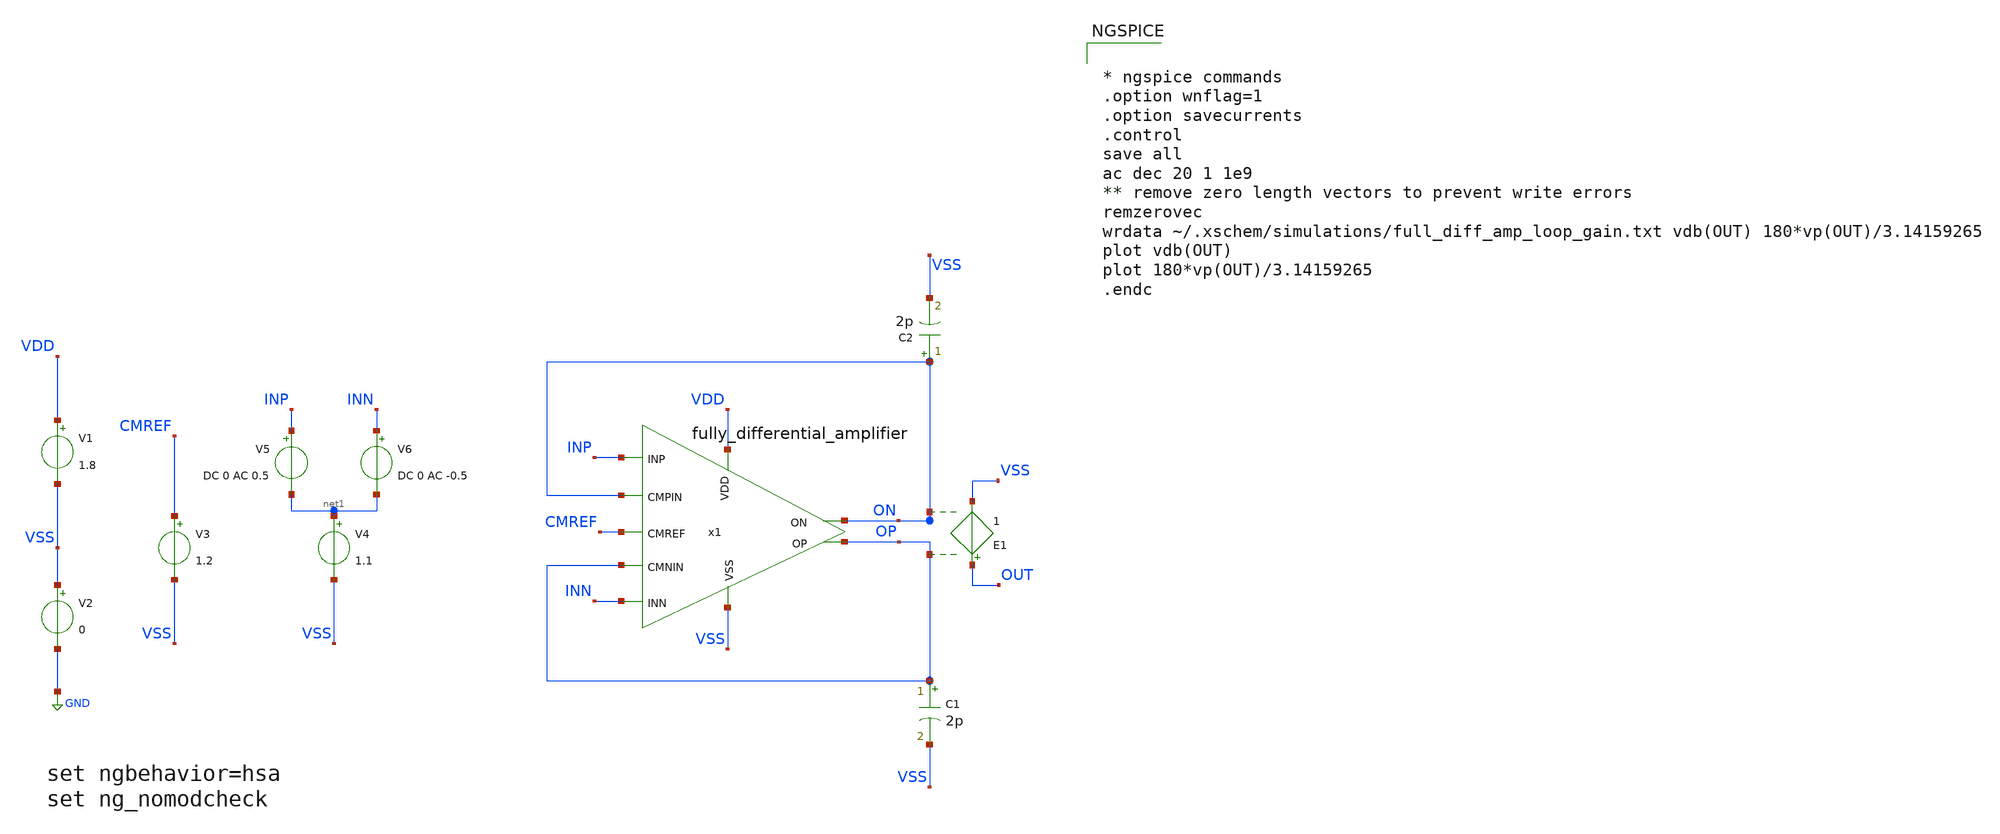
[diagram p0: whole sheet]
** sch_path: testbenches/full_diff_amp_loop_gain.sch
**.subckt full_diff_amp_loop_gain
x1 VDD ON INP OP INN ON OP CMREF VSS fully_differential_amplifier
V1 VDD VSS 1.8
V2 VSS GND 0
V3 CMREF VSS 1.2
V4 net1 VSS 1.1
V5 INP net1 DC 0 AC 0.5
V6 INN net1 DC 0 AC -0.5
E1 OUT VSS OP ON 1
C1 OP VSS 2p m=1
C2 ON VSS 2p m=1
**** begin user architecture code

** opencircuitdesign pdks install
.lib /foss/pdks/sky130A/libs.tech/combined/sky130.corners.lib.spice fslh



* ngspice commands
.option wnflag=1
.option savecurrents
.control
save all
ac dec 20 1 1e9
** remove zero length vectors to prevent write errors
remzerovec
wrdata ~/.xschem/simulations/full_diff_amp_loop_gain.txt vdb(OUT) 180*vp(OUT)/3.14159265
plot vdb(OUT)
plot 180*vp(OUT)/3.14159265
.endc



.control
begin
    let x1 = v(OUT)
    let x = db(x1[0])-3
    let y = db(x1)
    let l = length(y)-1
    let lpv = 0
    let tol = 0
    set units=degrees
    set do_again = 1

    while ($do_again eq 1)
        while (lpv lt l)
            let lpv = lpv+1
            if (abs(y[lpv]-x) lt tol)
                let threedB = mag(frequency[lpv])
                set do_again = 0
            end
        end
        if ($do_again eq 1)
            let tol = tol+0.1
            let lpv = 0
        end
    end
    let tol = 0
    set do_again = 1
    while ($do_again eq 1)
        while (lpv lt l)
            let lpv = lpv+1
            if (abs(y[lpv]) lt tol)
                let UGB = mag(frequency[lpv])
                let PM = 180 + ph(x1[lpv])
                set do_again = 0
            end
        end
        if ($do_again eq 1)
            let tol = tol+0.1
            let lpv = 0
        end
    end

    let DC_Gain = db(x1[0])
    print DC_Gain
    print threedB
    print UGB
    print PM

    label BOTTOM
    unlet x1 x y l lpv threedB UGB DC_Gain PM tol
    unset do_again
end
op
remzerovec
write ~/.xschem/simulations/full_diff_amp_loop_gain.raw
.endc


**** end user architecture code
**.ends

* expanding   symbol:  /foss/designs/sky130_analog_labs/designs/fully_differential_amplifier.sym #
*+ of pins=9
** sym_path: designs/fully_differential_amplifier.sym
** sch_path: designs/fully_differential_amplifier.sch
.subckt fully_differential_amplifier VDD ON INP OP INN CMPIN CMNIN CMREF VSS
*.ipin INP
*.ipin INN
*.ipin VDD
*.ipin VSS
*.opin OP
*.opin ON
*.ipin CMPIN
*.ipin CMNIN
*.ipin CMREF
XM1 net3 PBIAS VDD VDD sky130_fd_pr__pfet_01v8_lvt L=6 W=36 nf=1 ad='int((nf+1)/2) * W/nf * 0.29' as='int((nf+2)/2) * W/nf * 0.29'
+ pd='2*int((nf+1)/2) * (W/nf + 0.29)' ps='2*int((nf+2)/2) * (W/nf + 0.29)' nrd='0.29 / W' nrs='0.29 / W'
+ sa=0 sb=0 sd=0 mult=1 m=1
XM2 net2 PBIAS VDD VDD sky130_fd_pr__pfet_01v8_lvt L=6 W=36 nf=1 ad='int((nf+1)/2) * W/nf * 0.29' as='int((nf+2)/2) * W/nf * 0.29'
+ pd='2*int((nf+1)/2) * (W/nf + 0.29)' ps='2*int((nf+2)/2) * (W/nf + 0.29)' nrd='0.29 / W' nrs='0.29 / W'
+ sa=0 sb=0 sd=0 mult=1 m=1
XQ1 net6 net8 net1 VSS sky130_fd_pr__npn_05v5_w1p00l2p00
XQ2 net5 net8 VSS VSS sky130_fd_pr__npn_05v5_w1p00l2p00
XR1 VSS net1 VSS sky130_fd_pr__res_high_po_1p41 L=260 mult=1 m=1
XM3 PBIAS PCAS net3 VDD sky130_fd_pr__pfet_01v8_lvt L=6 W=36 nf=1 ad='int((nf+1)/2) * W/nf * 0.29' as='int((nf+2)/2) * W/nf * 0.29'
+ pd='2*int((nf+1)/2) * (W/nf + 0.29)' ps='2*int((nf+2)/2) * (W/nf + 0.29)' nrd='0.29 / W' nrs='0.29 / W'
+ sa=0 sb=0 sd=0 mult=4 m=4
XM7 net4 PCAS net2 VDD sky130_fd_pr__pfet_01v8_lvt L=6 W=36 nf=1 ad='int((nf+1)/2) * W/nf * 0.29' as='int((nf+2)/2) * W/nf * 0.29'
+ pd='2*int((nf+1)/2) * (W/nf + 0.29)' ps='2*int((nf+2)/2) * (W/nf + 0.29)' nrd='0.29 / W' nrs='0.29 / W'
+ sa=0 sb=0 sd=0 mult=4 m=4
XR7 PCAS PBIAS VSS sky130_fd_pr__res_high_po_1p41 L=600 mult=1 m=1
XR8 net7 net4 VSS sky130_fd_pr__res_high_po_1p41 L=600 mult=1 m=1
XM16 net7 net8 net5 VSS sky130_fd_pr__nfet_05v0_nvt L=2 W=10 nf=1 ad='int((nf+1)/2) * W/nf * 0.29' as='int((nf+2)/2) * W/nf * 0.29'
+ pd='2*int((nf+1)/2) * (W/nf + 0.29)' ps='2*int((nf+2)/2) * (W/nf + 0.29)' nrd='0.29 / W' nrs='0.29 / W'
+ sa=0 sb=0 sd=0 mult=6 m=6
XM18 PCAS net8 net6 VSS sky130_fd_pr__nfet_05v0_nvt L=2 W=10 nf=1 ad='int((nf+1)/2) * W/nf * 0.29' as='int((nf+2)/2) * W/nf * 0.29'
+ pd='2*int((nf+1)/2) * (W/nf + 0.29)' ps='2*int((nf+2)/2) * (W/nf + 0.29)' nrd='0.29 / W' nrs='0.29 / W'
+ sa=0 sb=0 sd=0 mult=6 m=6
XM19 VDD net7 net8 VSS sky130_fd_pr__nfet_05v0_nvt L=2 W=10 nf=1 ad='int((nf+1)/2) * W/nf * 0.29' as='int((nf+2)/2) * W/nf * 0.29'
+ pd='2*int((nf+1)/2) * (W/nf + 0.29)' ps='2*int((nf+2)/2) * (W/nf + 0.29)' nrd='0.29 / W' nrs='0.29 / W'
+ sa=0 sb=0 sd=0 mult=1 m=1
XM17 net11 PBIAS VDD VDD sky130_fd_pr__pfet_01v8_lvt L=6 W=36 nf=1 ad='int((nf+1)/2) * W/nf * 0.29' as='int((nf+2)/2) * W/nf * 0.29'
+ pd='2*int((nf+1)/2) * (W/nf + 0.29)' ps='2*int((nf+2)/2) * (W/nf + 0.29)' nrd='0.29 / W' nrs='0.29 / W'
+ sa=0 sb=0 sd=0 mult=1 m=1
XM20 net9 net11 PBIAS VDD sky130_fd_pr__pfet_01v8_lvt L=6 W=10 nf=1 ad='int((nf+1)/2) * W/nf * 0.29'
+ as='int((nf+2)/2) * W/nf * 0.29' pd='2*int((nf+1)/2) * (W/nf + 0.29)' ps='2*int((nf+2)/2) * (W/nf + 0.29)'
+ nrd='0.29 / W' nrs='0.29 / W' sa=0 sb=0 sd=0 mult=1 m=1
XM21 VSS net10 net9 VDD sky130_fd_pr__pfet_01v8_lvt L=6 W=10 nf=1 ad='int((nf+1)/2) * W/nf * 0.29' as='int((nf+2)/2) * W/nf * 0.29'
+ pd='2*int((nf+1)/2) * (W/nf + 0.29)' ps='2*int((nf+2)/2) * (W/nf + 0.29)' nrd='0.29 / W' nrs='0.29 / W'
+ sa=0 sb=0 sd=0 mult=1 m=1
XR10 net10 net11 VSS sky130_fd_pr__res_xhigh_po_0p35 L=350 mult=1 m=1
XR11 VSS net10 VSS sky130_fd_pr__res_xhigh_po_0p35 L=350 mult=1 m=1
XM4 net17 PBIAS VDD VDD sky130_fd_pr__pfet_01v8_lvt L=6 W=36 nf=1 ad='int((nf+1)/2) * W/nf * 0.29' as='int((nf+2)/2) * W/nf * 0.29'
+ pd='2*int((nf+1)/2) * (W/nf + 0.29)' ps='2*int((nf+2)/2) * (W/nf + 0.29)' nrd='0.29 / W' nrs='0.29 / W'
+ sa=0 sb=0 sd=0 mult=1 m=1
XM5 NCAS PCAS net17 VDD sky130_fd_pr__pfet_01v8_lvt L=6 W=36 nf=1 ad='int((nf+1)/2) * W/nf * 0.29' as='int((nf+2)/2) * W/nf * 0.29'
+ pd='2*int((nf+1)/2) * (W/nf + 0.29)' ps='2*int((nf+2)/2) * (W/nf + 0.29)' nrd='0.29 / W' nrs='0.29 / W'
+ sa=0 sb=0 sd=0 mult=4 m=4
XR2 NBIAS NCAS VSS sky130_fd_pr__res_high_po_1p41 L=600 mult=1 m=1
XM6 NBIAS NCAS net12 VSS sky130_fd_pr__nfet_01v8 L=6 W=36 nf=1 ad='int((nf+1)/2) * W/nf * 0.29' as='int((nf+2)/2) * W/nf * 0.29'
+ pd='2*int((nf+1)/2) * (W/nf + 0.29)' ps='2*int((nf+2)/2) * (W/nf + 0.29)' nrd='0.29 / W' nrs='0.29 / W'
+ sa=0 sb=0 sd=0 mult=4 m=4
XM8 net12 NBIAS VSS VSS sky130_fd_pr__nfet_01v8 L=6 W=36 nf=1 ad='int((nf+1)/2) * W/nf * 0.29' as='int((nf+2)/2) * W/nf * 0.29'
+ pd='2*int((nf+1)/2) * (W/nf + 0.29)' ps='2*int((nf+2)/2) * (W/nf + 0.29)' nrd='0.29 / W' nrs='0.29 / W'
+ sa=0 sb=0 sd=0 mult=1 m=1
XM9 net18 INN net14 VSS sky130_fd_pr__nfet_01v8 L=1 W=150 nf=1 ad='int((nf+1)/2) * W/nf * 0.29' as='int((nf+2)/2) * W/nf * 0.29'
+ pd='2*int((nf+1)/2) * (W/nf + 0.29)' ps='2*int((nf+2)/2) * (W/nf + 0.29)' nrd='0.29 / W' nrs='0.29 / W'
+ sa=0 sb=0 sd=0 mult=2 m=2
XM10 net19 INP net14 VSS sky130_fd_pr__nfet_01v8 L=1 W=150 nf=1 ad='int((nf+1)/2) * W/nf * 0.29' as='int((nf+2)/2) * W/nf * 0.29'
+ pd='2*int((nf+1)/2) * (W/nf + 0.29)' ps='2*int((nf+2)/2) * (W/nf + 0.29)' nrd='0.29 / W' nrs='0.29 / W'
+ sa=0 sb=0 sd=0 mult=2 m=2
XM11 net14 NCAS net13 VSS sky130_fd_pr__nfet_01v8 L=6 W=36 nf=1 ad='int((nf+1)/2) * W/nf * 0.29' as='int((nf+2)/2) * W/nf * 0.29'
+ pd='2*int((nf+1)/2) * (W/nf + 0.29)' ps='2*int((nf+2)/2) * (W/nf + 0.29)' nrd='0.29 / W' nrs='0.29 / W'
+ sa=0 sb=0 sd=0 mult=84 m=84
XM12 net13 NBIAS VSS VSS sky130_fd_pr__nfet_01v8 L=6 W=36 nf=1 ad='int((nf+1)/2) * W/nf * 0.29' as='int((nf+2)/2) * W/nf * 0.29'
+ pd='2*int((nf+1)/2) * (W/nf + 0.29)' ps='2*int((nf+2)/2) * (W/nf + 0.29)' nrd='0.29 / W' nrs='0.29 / W'
+ sa=0 sb=0 sd=0 mult=21 m=21
XM13 ON NCAS net15 VSS sky130_fd_pr__nfet_01v8 L=6 W=36 nf=1 ad='int((nf+1)/2) * W/nf * 0.29' as='int((nf+2)/2) * W/nf * 0.29'
+ pd='2*int((nf+1)/2) * (W/nf + 0.29)' ps='2*int((nf+2)/2) * (W/nf + 0.29)' nrd='0.29 / W' nrs='0.29 / W'
+ sa=0 sb=0 sd=0 mult=16 m=16
XM14 net15 NBIAS VSS VSS sky130_fd_pr__nfet_01v8 L=6 W=36 nf=1 ad='int((nf+1)/2) * W/nf * 0.29' as='int((nf+2)/2) * W/nf * 0.29'
+ pd='2*int((nf+1)/2) * (W/nf + 0.29)' ps='2*int((nf+2)/2) * (W/nf + 0.29)' nrd='0.29 / W' nrs='0.29 / W'
+ sa=0 sb=0 sd=0 mult=4 m=4
XM15 OP NCAS net16 VSS sky130_fd_pr__nfet_01v8 L=6 W=36 nf=1 ad='int((nf+1)/2) * W/nf * 0.29' as='int((nf+2)/2) * W/nf * 0.29'
+ pd='2*int((nf+1)/2) * (W/nf + 0.29)' ps='2*int((nf+2)/2) * (W/nf + 0.29)' nrd='0.29 / W' nrs='0.29 / W'
+ sa=0 sb=0 sd=0 mult=16 m=16
XM22 net16 NBIAS VSS VSS sky130_fd_pr__nfet_01v8 L=6 W=36 nf=1 ad='int((nf+1)/2) * W/nf * 0.29' as='int((nf+2)/2) * W/nf * 0.29'
+ pd='2*int((nf+1)/2) * (W/nf + 0.29)' ps='2*int((nf+2)/2) * (W/nf + 0.29)' nrd='0.29 / W' nrs='0.29 / W'
+ sa=0 sb=0 sd=0 mult=4 m=4
XM23 net18 CMFB VDD VDD sky130_fd_pr__pfet_01v8_lvt L=6 W=36 nf=1 ad='int((nf+1)/2) * W/nf * 0.29' as='int((nf+2)/2) * W/nf * 0.29'
+ pd='2*int((nf+1)/2) * (W/nf + 0.29)' ps='2*int((nf+2)/2) * (W/nf + 0.29)' nrd='0.29 / W' nrs='0.29 / W'
+ sa=0 sb=0 sd=0 mult=15 m=15
XM24 OP PCAS net18 VDD sky130_fd_pr__pfet_01v8_lvt L=6 W=36 nf=1 ad='int((nf+1)/2) * W/nf * 0.29' as='int((nf+2)/2) * W/nf * 0.29'
+ pd='2*int((nf+1)/2) * (W/nf + 0.29)' ps='2*int((nf+2)/2) * (W/nf + 0.29)' nrd='0.29 / W' nrs='0.29 / W'
+ sa=0 sb=0 sd=0 mult=16 m=16
XM25 net19 CMFB VDD VDD sky130_fd_pr__pfet_01v8_lvt L=6 W=36 nf=1 ad='int((nf+1)/2) * W/nf * 0.29' as='int((nf+2)/2) * W/nf * 0.29'
+ pd='2*int((nf+1)/2) * (W/nf + 0.29)' ps='2*int((nf+2)/2) * (W/nf + 0.29)' nrd='0.29 / W' nrs='0.29 / W'
+ sa=0 sb=0 sd=0 mult=15 m=15
XM26 ON PCAS net19 VDD sky130_fd_pr__pfet_01v8_lvt L=6 W=36 nf=1 ad='int((nf+1)/2) * W/nf * 0.29' as='int((nf+2)/2) * W/nf * 0.29'
+ pd='2*int((nf+1)/2) * (W/nf + 0.29)' ps='2*int((nf+2)/2) * (W/nf + 0.29)' nrd='0.29 / W' nrs='0.29 / W'
+ sa=0 sb=0 sd=0 mult=16 m=16
XM27 net20 NBIAS VSS VSS sky130_fd_pr__nfet_01v8 L=6 W=36 nf=1 ad='int((nf+1)/2) * W/nf * 0.29' as='int((nf+2)/2) * W/nf * 0.29'
+ pd='2*int((nf+1)/2) * (W/nf + 0.29)' ps='2*int((nf+2)/2) * (W/nf + 0.29)' nrd='0.29 / W' nrs='0.29 / W'
+ sa=0 sb=0 sd=0 mult=2 m=2
XM28 net21 NBIAS VSS VSS sky130_fd_pr__nfet_01v8 L=6 W=36 nf=1 ad='int((nf+1)/2) * W/nf * 0.29' as='int((nf+2)/2) * W/nf * 0.29'
+ pd='2*int((nf+1)/2) * (W/nf + 0.29)' ps='2*int((nf+2)/2) * (W/nf + 0.29)' nrd='0.29 / W' nrs='0.29 / W'
+ sa=0 sb=0 sd=0 mult=2 m=2
XM29 net22 NCAS net20 VSS sky130_fd_pr__nfet_01v8 L=6 W=36 nf=1 ad='int((nf+1)/2) * W/nf * 0.29' as='int((nf+2)/2) * W/nf * 0.29'
+ pd='2*int((nf+1)/2) * (W/nf + 0.29)' ps='2*int((nf+2)/2) * (W/nf + 0.29)' nrd='0.29 / W' nrs='0.29 / W'
+ sa=0 sb=0 sd=0 mult=8 m=8
XM30 net23 NCAS net21 VSS sky130_fd_pr__nfet_01v8 L=6 W=36 nf=1 ad='int((nf+1)/2) * W/nf * 0.29' as='int((nf+2)/2) * W/nf * 0.29'
+ pd='2*int((nf+1)/2) * (W/nf + 0.29)' ps='2*int((nf+2)/2) * (W/nf + 0.29)' nrd='0.29 / W' nrs='0.29 / W'
+ sa=0 sb=0 sd=0 mult=8 m=8
XM31 CMFB CMREF net22 VSS sky130_fd_pr__nfet_01v8 L=1 W=5 nf=1 ad='int((nf+1)/2) * W/nf * 0.29' as='int((nf+2)/2) * W/nf * 0.29'
+ pd='2*int((nf+1)/2) * (W/nf + 0.29)' ps='2*int((nf+2)/2) * (W/nf + 0.29)' nrd='0.29 / W' nrs='0.29 / W'
+ sa=0 sb=0 sd=0 mult=1 m=1
XM32 net24 CMPIN net22 VSS sky130_fd_pr__nfet_01v8 L=1 W=5 nf=1 ad='int((nf+1)/2) * W/nf * 0.29' as='int((nf+2)/2) * W/nf * 0.29'
+ pd='2*int((nf+1)/2) * (W/nf + 0.29)' ps='2*int((nf+2)/2) * (W/nf + 0.29)' nrd='0.29 / W' nrs='0.29 / W'
+ sa=0 sb=0 sd=0 mult=1 m=1
XM33 net24 CMNIN net23 VSS sky130_fd_pr__nfet_01v8 L=1 W=5 nf=1 ad='int((nf+1)/2) * W/nf * 0.29' as='int((nf+2)/2) * W/nf * 0.29'
+ pd='2*int((nf+1)/2) * (W/nf + 0.29)' ps='2*int((nf+2)/2) * (W/nf + 0.29)' nrd='0.29 / W' nrs='0.29 / W'
+ sa=0 sb=0 sd=0 mult=1 m=1
XM34 CMFB CMREF net23 VSS sky130_fd_pr__nfet_01v8 L=1 W=5 nf=1 ad='int((nf+1)/2) * W/nf * 0.29' as='int((nf+2)/2) * W/nf * 0.29'
+ pd='2*int((nf+1)/2) * (W/nf + 0.29)' ps='2*int((nf+2)/2) * (W/nf + 0.29)' nrd='0.29 / W' nrs='0.29 / W'
+ sa=0 sb=0 sd=0 mult=1 m=1
XM35 CMFB net24 VDD VDD sky130_fd_pr__pfet_01v8_lvt L=6 W=36 nf=1 ad='int((nf+1)/2) * W/nf * 0.29' as='int((nf+2)/2) * W/nf * 0.29'
+ pd='2*int((nf+1)/2) * (W/nf + 0.29)' ps='2*int((nf+2)/2) * (W/nf + 0.29)' nrd='0.29 / W' nrs='0.29 / W'
+ sa=0 sb=0 sd=0 mult=4 m=4
XM36 net24 net24 VDD VDD sky130_fd_pr__pfet_01v8_lvt L=6 W=36 nf=1 ad='int((nf+1)/2) * W/nf * 0.29' as='int((nf+2)/2) * W/nf * 0.29'
+ pd='2*int((nf+1)/2) * (W/nf + 0.29)' ps='2*int((nf+2)/2) * (W/nf + 0.29)' nrd='0.29 / W' nrs='0.29 / W'
+ sa=0 sb=0 sd=0 mult=2 m=2
XM37 net24 net24 VDD VDD sky130_fd_pr__pfet_01v8_lvt L=6 W=36 nf=1 ad='int((nf+1)/2) * W/nf * 0.29' as='int((nf+2)/2) * W/nf * 0.29'
+ pd='2*int((nf+1)/2) * (W/nf + 0.29)' ps='2*int((nf+2)/2) * (W/nf + 0.29)' nrd='0.29 / W' nrs='0.29 / W'
+ sa=0 sb=0 sd=0 mult=2 m=2
XC1 CMFB ON VSS sky130_fd_pr__cap_var_lvt W=30 L=30 VM=1 m=1
XC2 CMFB OP VSS sky130_fd_pr__cap_var_lvt W=30 L=30 VM=1 m=1
.ends

.GLOBAL GND
.end
